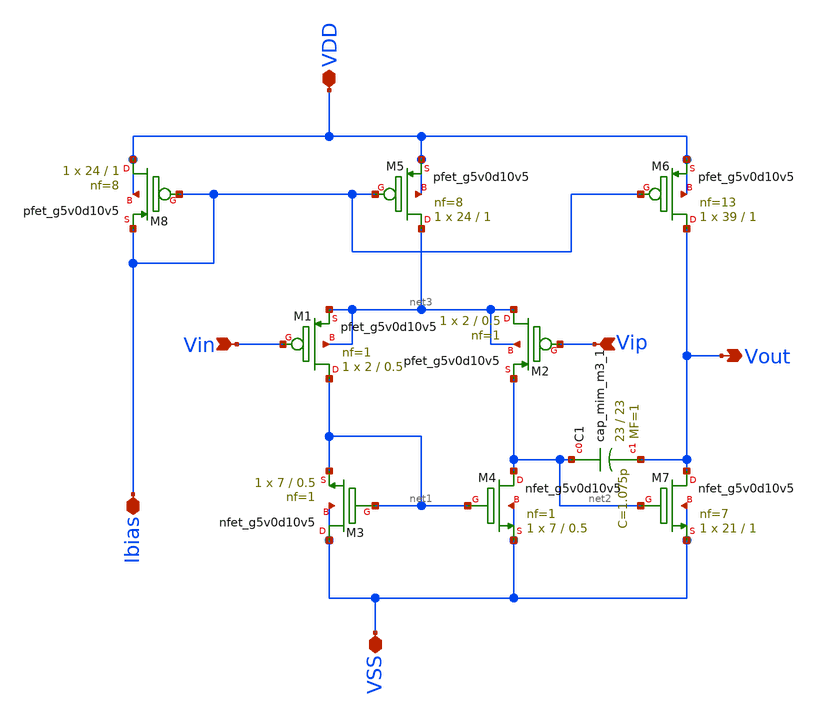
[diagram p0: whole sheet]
** sch_path: xschem/Ota_esq.sch
**.subckt Ota_esq Vin Vip VDD VSS Ibias Vout
*.ipin Vin
*.ipin Vip
*.iopin VDD
*.iopin VSS
*.iopin Ibias
*.opin Vout
XC1 net2 Vout sky130_fd_pr__cap_mim_m3_1 W=23 L=23 MF=1 m=1
XM3 VSS net1 net1 VSS sky130_fd_pr__nfet_g5v0d10v5 L=0.5 W=7 nf=1 ad='int((nf+1)/2) * W/nf * 0.29' as='int((nf+2)/2) * W/nf * 0.29'
+ pd='2*int((nf+1)/2) * (W/nf + 0.29)' ps='2*int((nf+2)/2) * (W/nf + 0.29)' nrd='0.29 / W' nrs='0.29 / W'
+ sa=0 sb=0 sd=0 mult=1 m=1
XM1 net1 Vin net3 net3 sky130_fd_pr__pfet_g5v0d10v5 L=0.5 W=2 nf=1 ad='int((nf+1)/2) * W/nf * 0.29' as='int((nf+2)/2) * W/nf * 0.29'
+ pd='2*int((nf+1)/2) * (W/nf + 0.29)' ps='2*int((nf+2)/2) * (W/nf + 0.29)' nrd='0.29 / W' nrs='0.29 / W'
+ sa=0 sb=0 sd=0 mult=1 m=1
XM2 net3 Vip net2 net3 sky130_fd_pr__pfet_g5v0d10v5 L=0.5 W=2 nf=1 ad='int((nf+1)/2) * W/nf * 0.29' as='int((nf+2)/2) * W/nf * 0.29'
+ pd='2*int((nf+1)/2) * (W/nf + 0.29)' ps='2*int((nf+2)/2) * (W/nf + 0.29)' nrd='0.29 / W' nrs='0.29 / W'
+ sa=0 sb=0 sd=0 mult=1 m=1
XM4 net2 net1 VSS VSS sky130_fd_pr__nfet_g5v0d10v5 L=0.5 W=7 nf=1 ad='int((nf+1)/2) * W/nf * 0.29' as='int((nf+2)/2) * W/nf * 0.29'
+ pd='2*int((nf+1)/2) * (W/nf + 0.29)' ps='2*int((nf+2)/2) * (W/nf + 0.29)' nrd='0.29 / W' nrs='0.29 / W'
+ sa=0 sb=0 sd=0 mult=1 m=1
XM7 Vout net2 VSS VSS sky130_fd_pr__nfet_g5v0d10v5 L=1 W=21 nf=7 ad='int((nf+1)/2) * W/nf * 0.29' as='int((nf+2)/2) * W/nf * 0.29'
+ pd='2*int((nf+1)/2) * (W/nf + 0.29)' ps='2*int((nf+2)/2) * (W/nf + 0.29)' nrd='0.29 / W' nrs='0.29 / W'
+ sa=0 sb=0 sd=0 mult=1 m=1
XM8 VDD Ibias Ibias VDD sky130_fd_pr__pfet_g5v0d10v5 L=1 W=24 nf=8 ad='int((nf+1)/2) * W/nf * 0.29' as='int((nf+2)/2) * W/nf * 0.29'
+ pd='2*int((nf+1)/2) * (W/nf + 0.29)' ps='2*int((nf+2)/2) * (W/nf + 0.29)' nrd='0.29 / W' nrs='0.29 / W'
+ sa=0 sb=0 sd=0 mult=1 m=1
XM5 net3 Ibias VDD VDD sky130_fd_pr__pfet_g5v0d10v5 L=1 W=24 nf=8 ad='int((nf+1)/2) * W/nf * 0.29' as='int((nf+2)/2) * W/nf * 0.29'
+ pd='2*int((nf+1)/2) * (W/nf + 0.29)' ps='2*int((nf+2)/2) * (W/nf + 0.29)' nrd='0.29 / W' nrs='0.29 / W'
+ sa=0 sb=0 sd=0 mult=1 m=1
XM6 Vout Ibias VDD VDD sky130_fd_pr__pfet_g5v0d10v5 L=1 W=39 nf=13 ad='int((nf+1)/2) * W/nf * 0.29' as='int((nf+2)/2) * W/nf * 0.29'
+ pd='2*int((nf+1)/2) * (W/nf + 0.29)' ps='2*int((nf+2)/2) * (W/nf + 0.29)' nrd='0.29 / W' nrs='0.29 / W'
+ sa=0 sb=0 sd=0 mult=1 m=1
**.ends
.end
